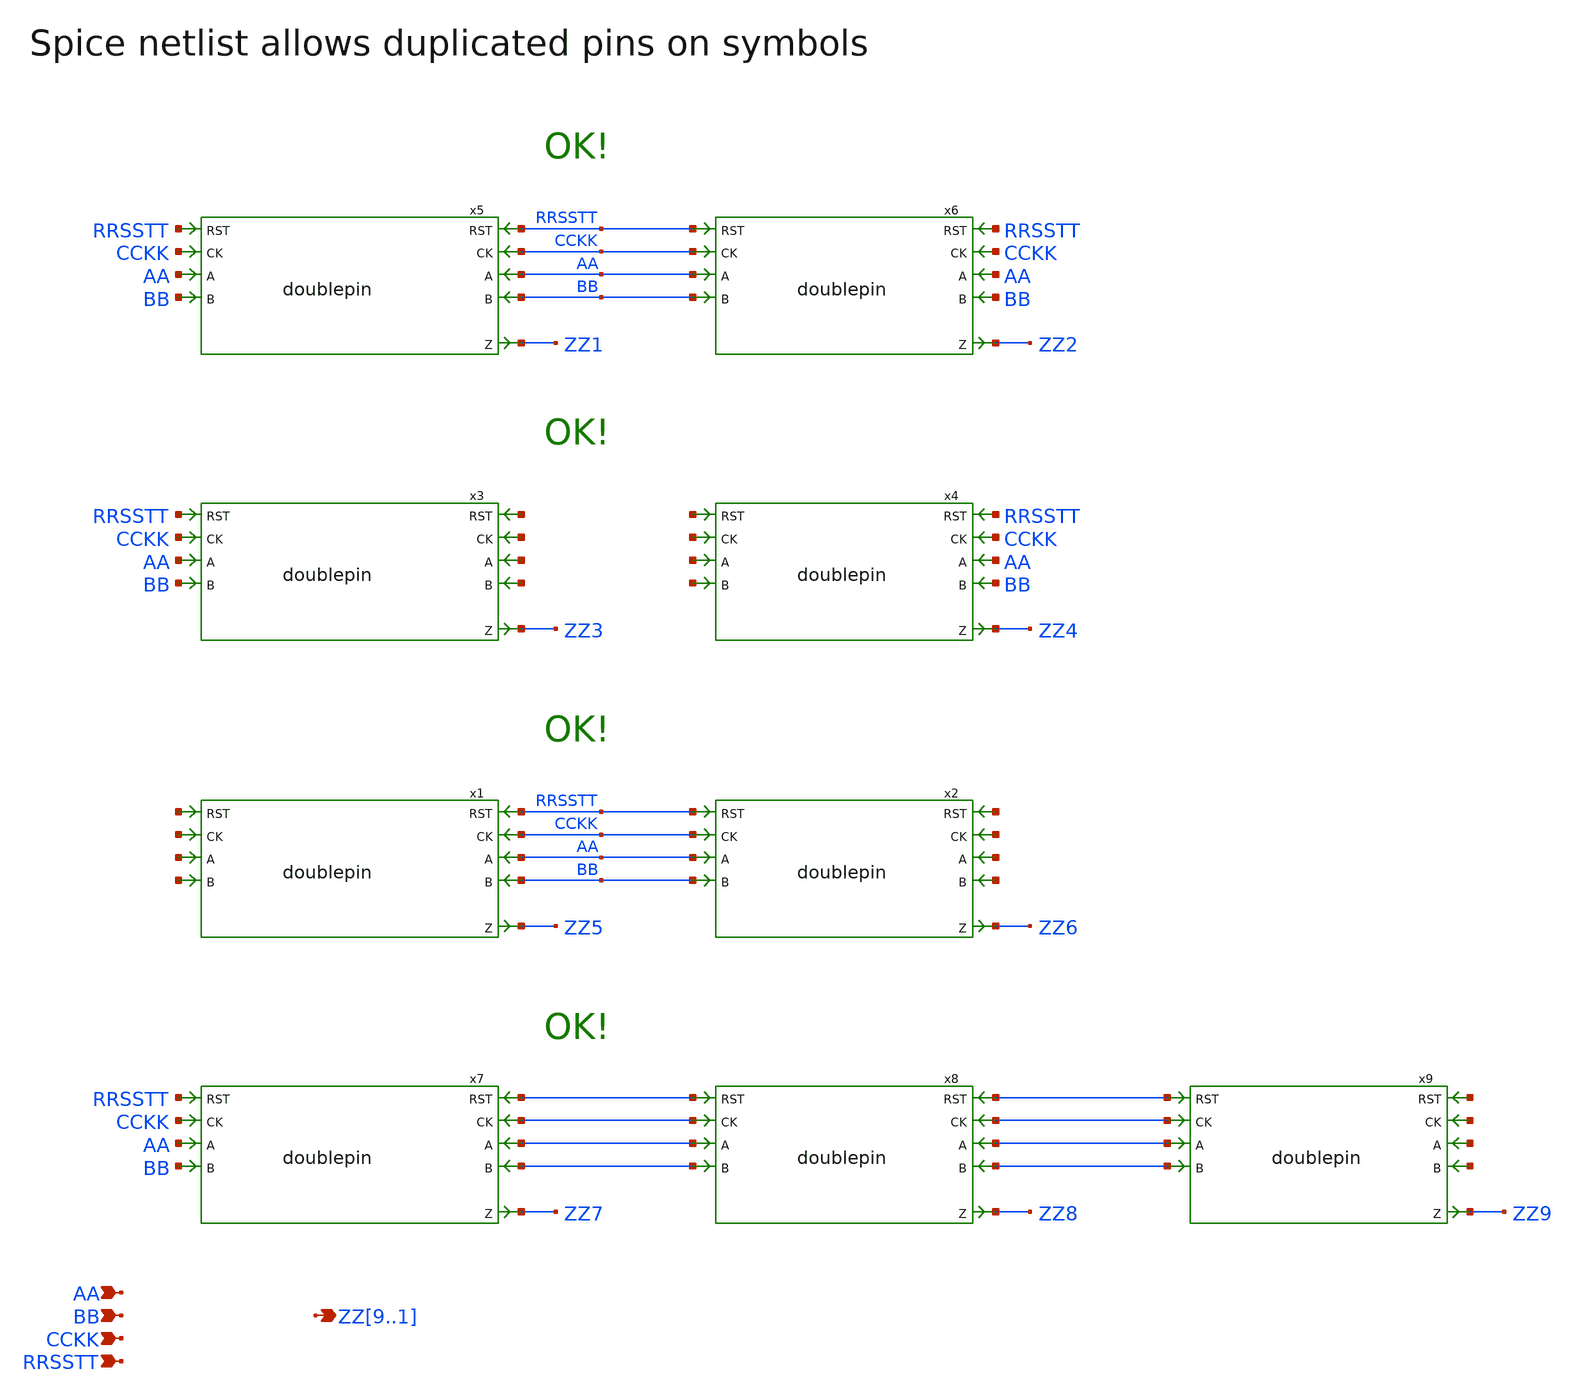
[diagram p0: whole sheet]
** sch_path: xschem_library/examples/test_doublepin.sch
**.subckt test_doublepin RRSSTT CCKK BB AA ZZ9,ZZ8,ZZ7,ZZ6,ZZ5,ZZ4,ZZ3,ZZ2,ZZ1
*.ipin RRSSTT
*.ipin CCKK
*.ipin BB
*.ipin AA
*.opin ZZ9,ZZ8,ZZ7,ZZ6,ZZ5,ZZ4,ZZ3,ZZ2,ZZ1
x9 AA BB CCKK RRSSTT ZZ9 doublepin
x8 AA BB CCKK RRSSTT ZZ8 doublepin
x2 AA BB CCKK RRSSTT ZZ6 doublepin
x3 AA BB CCKK RRSSTT ZZ3 doublepin
x4 AA BB CCKK RRSSTT ZZ4 doublepin
x5 AA BB CCKK RRSSTT ZZ1 doublepin
x6 AA BB CCKK RRSSTT ZZ2 doublepin
x1 AA BB CCKK RRSSTT ZZ5 doublepin
x7 AA BB CCKK RRSSTT ZZ7 doublepin
**** begin user architecture code
va a 0 pwl 0 0 100n 0 101n 3
vvcc vcc 0 dc 3
vvss vss 0 dc 0

.tran 1n 200n
**** end user architecture code
**.ends

* expanding   symbol:  doublepin.sym # of pins=9
** sym_path: xschem_library/examples/doublepin.sym
** sch_path: xschem_library/examples/doublepin.sch
.subckt doublepin A B CK RST Z
*.ipin A
*.ipin B
*.opin Z
*.ipin RST
*.ipin CK
* noconn CK
* noconn RST
* noconn A
* noconn B
* noconn Z
.ends

.end
